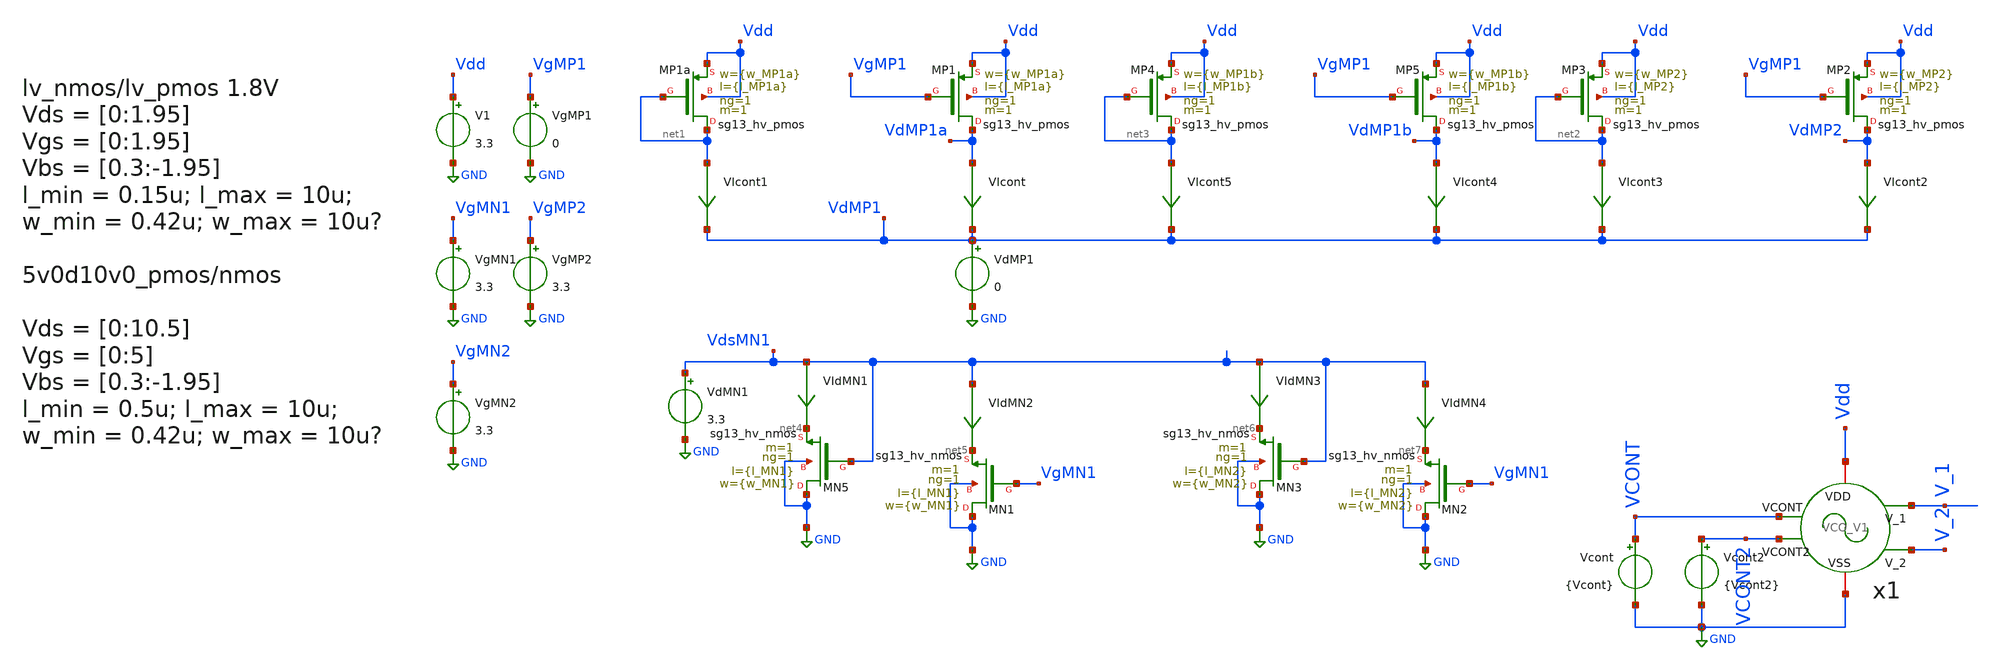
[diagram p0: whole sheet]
** sch_path: xschem/VCO/TB_VCO_Design_V1.sch
**.subckt TB_VCO_Design_V1
V1 Vdd GND 3.3
VIcont VdMP1a VdMP1 0
.save i(vicont)
VdMP1 VdMP1 GND 0
VgMP1 VgMP1 GND 0
VdMN1 VdsMN1 GND 3.3
VIdMN1 VdsMN1 net4 0
.save i(vidmn1)
VIcont1 net1 VdMP1 0
.save i(vicont1)
VIdMN2 VdsMN1 net5 0
.save i(vidmn2)
VgMN1 VgMN1 GND 3.3
VIdMN3 VdsMN1 net6 0
.save i(vidmn3)
VIdMN4 VdsMN1 net7 0
.save i(vidmn4)
VIcont2 VdMP2 VdMP1 0
.save i(vicont2)
VIcont3 net2 VdMP1 0
.save i(vicont3)
VgMP2 VgMP2 GND 3.3
VgMN2 VgMN2 GND 3.3
Vcont VCONT GND {Vcont}
XMP1a net1 net1 Vdd Vdd sg13_hv_pmos w={w_MP1a} l={l_MP1a} ng=1 m=1 mm_ok=1
XMP1 VdMP1a VgMP1 Vdd Vdd sg13_hv_pmos w={w_MP1a} l={l_MP1a} ng=1 m=1 mm_ok=1
XMP3 net2 net2 Vdd Vdd sg13_hv_pmos w={w_MP2} l={l_MP2} ng=1 m=1 mm_ok=1
XMP2 VdMP2 VgMP1 Vdd Vdd sg13_hv_pmos w={w_MP2} l={l_MP2} ng=1 m=1 mm_ok=1
XMN5 GND VdsMN1 net4 GND sg13_hv_nmos w={w_MN1} l={l_MN1} ng=1 m=1 mm_ok=1
XMN1 GND VgMN1 net5 GND sg13_hv_nmos w={w_MN1} l={l_MN1} ng=1 m=1 mm_ok=1
XMN3 GND VdsMN1 net6 GND sg13_hv_nmos w={w_MN2} l={l_MN2} ng=1 m=1 mm_ok=1
XMN2 GND VgMN1 net7 GND sg13_hv_nmos w={w_MN2} l={l_MN2} ng=1 m=1 mm_ok=1
VIcont4 VdMP1b VdMP1 0
.save i(vicont4)
VIcont5 net3 VdMP1 0
.save i(vicont5)
XMP4 net3 net3 Vdd Vdd sg13_hv_pmos w={w_MP1b} l={l_MP1b} ng=1 m=1 mm_ok=1
XMP5 VdMP1b VgMP1 Vdd Vdd sg13_hv_pmos w={w_MP1b} l={l_MP1b} ng=1 m=1 mm_ok=1
x1 VCONT GND Vdd V_1 V_2 VCONT2 VCO_V1
Vcont2 VCONT2 GND {Vcont2}
**** begin user architecture code


.save all


.csparam start = 10
.param Vcont = 1

.control

dc VdMP1 0 3.3 0.2 VgMP1 0 3.3 0.2
let IdMP1a = i(VIcont)
let IdMP1a_Diode = i(VIcont1)
let  VsdMP1 = v(Vdd) - v(VdMP1)
let VthMP1 = @n.xMP1.msky130_fd_pr__pfet_01v8[vth]
let  VovMP1a = v(Vdd) - v(VdMP1) - VthMP1
*plot IdMP1a IdMP1a_Diode vs VsdMP1
*plot IdMP1a_Diode vs VovMP1

let IdMP1b = i(VIcont4)
let IdMP1b_Diode = i(VIcont5)
let  VsdMP1 = v(Vdd) - v(VdMP1)
let VthMP1 = @n.xMP1.msky130_fd_pr__pfet_01v8[vth]
let  VovMP1b = v(Vdd) - v(VdMP1) - VthMP1
*plot IdMP1b IdMP1b_Diode vs VsdMP1
*plot IdMP1b_Diode vs VovMP1

let IdMP2 = i(VIcont2)
let IdMP2_Diode = i(VIcont3)
let  VsdMP2 = v(Vdd) - v(VdMP2)
let VthMP2 = @m.xMP4.msky130_fd_pr__pfet_01v8[vth]
let  VovMP2 = v(Vdd) - v(VdMP2) - VthMP2
*plot IdMP2 IdMP2_Diode vs VsdMP2
*plot IdMP2_Diode vs VovMP2
let KP1 = IdMP1_Diode/(VovMP1*VovMP1)
let AP1 = sqrt(KP1)
let KP2 = IdMP2_Diode/(VovMP2*VovMP2)
let AP2 = sqrt(KP2)

plot AP1 AP2

*plot IdMP1_Diode IdMP2_Diode vs VsdMP1
print VthMP1 VthMP2
*wrdata ../../sim_data/data_VCO_design.txt IdMP1_Diode VovMP1 IdMP1 vs VsdMP1
wrdata
+ /workspaces/usm-vlsi-tools/shared_xserver/simulations/SKY130/IPD500-TimebasedDCDCBuck/sim_data/data_VCO_design.txt IdMP1_Diode VovMP1 IdMP1 vs VsdMP1
wrdata
+ /workspaces/usm-vlsi-tools/shared_xserver/simulations/SKY130/IPD500-TimebasedDCDCBuck/sim_data/data_AP1_VthMP1.txt AP1 VthMP1 AP2 VthMP2

reset
*load save_data.raw
*show

dc VdMN1 0 3.3 0.2 VgMN1 0 3.3 0.2
let VdsMN1 = v(VdsMN1)
let IdMN1_Diode = i(VIdMN1)
let IdMN1 = i(VIdMN2)
let VthMN1 = @m.xMN1.msky130_fd_pr__nfet_01v8[vth]
let VovMN1 = VdsMN1 - VthMN1
*plot IdMN1 IdMN1_Diode vs VdsMN1
*plot IdMN1_Diode vs VovMN1

let VdsMN2 = v(VdsMN1)
let IdMN2_Diode = i(VIdMN3)
let IdMN2 = i(VIdMN4)
let VthMN2 = @m.xMN4.msky130_fd_pr__nfet_01v8[vth]
let VovMN2 = VdsMN2 - VthMN2
*plot IdMN2 IdMN2_Diode vs VdsMN2
*plot IdMN2_Diode vs VovMN2

let KN1 = IdMN1_Diode/(VovMN1*VovMN1)
let AN1 = sqrt(KN1)
let KN2 = IdMN2_Diode/(VovMN2*VovMN2)
let AN2 = sqrt(KN2)
*plot AN1 AN2
print VthMN1 VthMN2
wrdata
+ /workspaces/usm-vlsi-tools/shared_xserver/simulations/SKY130/IPD500-TimebasedDCDCBuck/sim_data/data_AN1_VthMN1.txt AN1 VthMN1


reset

dc Vcont 0 2 0.1
*dc Vcont 0 3 0.1
let Icont = i(v.x1.x1.VIcont)
let Icont2 = i(v.x1.x1.VIcont1)
let Icont3 = i(v.x1.x1.VIcont3)
let VCN = v(x1.x1.VCN)
let VCP = v(x1.x1.VCP)
let Vsg_MP3 = v(Vdd) - VCP
let VsdMP3 = v(VDD) - v(x1.x1.VSMP4)
let VdsMN3 = v(x1.x1.VdsMN3)


plot Icont Icont2 Icont3 vs Vcont
plot Icont3 vs Vcont
plot Icont3 vs VCP
plot VCP vs Vcont
plot VCN Vsg_MP3 vs Vcont
plot VsdMP3 VdsMN3 vs Vcont
*plot Vin vs Vcont
.endc





.lib cornerMOShv.lib mos_tt
.lib cornerMOSlv.lib mos_tt
*.lib cornerMOShv.lib mos_ff
*.lib cornerMOSlv.lib mos_ff
*.lib cornerMOShv.lib mos_ss
*.lib cornerMOSlv.lib mos_ss
*.lib cornerMOShv.lib mos_sf
*.lib cornerMOSlv.lib mos_sf
*.lib cornerMOShv.lib mos_fs
*.lib cornerMOSlv.lib mos_fs

*.include /opt/pdks/ihp-sg13g2/libs.ref/sg13g2_stdcell/spice/sg13g2_stdcell.spice
*.lib $::SG13G2_MODELS/cornerRES.lib res_typ
*.lib $::SG13G2_MODELS/cornerCAP.lib cap_typ
*.lib $::SG13G2_MODELS/diodes.lib


.param Vcont2 = 3.3

.param w_MP1a = 4u
.param l_MP1a = 7u
.param w_MP1b = 4u
.param l_MP1b = 7u
.param w_MP2 = 8u
.param l_MP2 = 4u
.param w_MP3 = 5u
.param l_MP3 = 4u
.param w_MP4 = 5u
.param l_MP4 = 5u

.param w_MN1 = 5u
.param l_MN1 = 0.5u
.param w_MN2 = 5u
.param l_MN2 = 0.5u
.param w_MN3 = 3u
.param l_MN3 = 0.5u
.param w_MN4 = 2u
.param l_MN4 = 5u





.save all
.param Vcont = 1

.control
reset
unset filetype
op
alter Vcont 1
let VCN = v(x1.x1.VCN)
let VCP = v(x1.x1.VCP)

let Vsd_MP4 = v(x1.x1.VSMP4) - v(x1.x1.VOUT)
let Vsd_MP3 = v(VDD) - v(x1.x1.VSMP4)
let Vsd_MP2 = v(VDD) - v(x1.x1.VCP)
let Vsd_MP1 = v(VDD) - VCN
let Vds_MN4 = v(x1.x1.VOUT) - v(x1.x1.VdsMN3)

let Vth_MP1a = @n.x1.x1.xmp1a.nsg13_hv_pmos[vth]
let Vth_MP1b = @n.x1.x1.xmp1b.nsg13_hv_pmos[vth]
let Vth_MP2 = @n.x1.x1.xmp2.nsg13_hv_pmos[vth]
let Vth_MP3 = @n.x1.x1.xmp3.nsg13_hv_pmos[vth]
let Vth_MP4 = @n.x1.x1.xmp3.nsg13_hv_pmos[vth]
let Vth_MN1 = @n.x1.x1.xmn1.nsg13_hv_nmos[vth]
let Vth_MN2 = @n.x1.x1.xmn2.nsg13_hv_nmos[vth]
let Vth_MN3 = @n.x1.x1.xmn3.nsg13_hv_nmos[vth]
let Vth_MN4 = @n.x1.x1.xmn4.nsg13_hv_nmos[vth]

let Vsg_MP4 = v(x1.x1.VSMP4) - v(x1.x1.VIN)
let Vsg_MP3 = v(VDD) - VCP
let Vsg_MP1a = v(VDD) - v(VCONT)
let Vsg_MP1b = v(VDD) - v(VCONT2)
let Vgs_MN4 = v(x1.x1.VIN) - v(x1.x1.VdsMN3)

let Vov_MP1a = Vsg_MP1a - Vth_MP1a
let Vov_MP1b = Vsg_MP1b - Vth_MP1b
let Vov_MP3 = Vsg_MP3 - Vth_MP3
let Vov_MP4 = Vsg_MP4 - Vth_MP4
let Vov_MN2 =  VCN - Vth_MN2
let Vov_MN3 =  VCN - Vth_MN3
let Vov_MN4 =  VCN - Vth_MN4

let gds_MN3 = @n.x1.x1.xmn3.nsg13_hv_nmos[gds]
let Ron_MN3 = 1/gds_MN3
let gds_MP3 = @n.x1.x1.xmp3.nsg13_hv_pmos[gds]
let Ron_MP3 = 1/gds_MP3


write TB_VCO_Design_V1.raw
.endc



**** end user architecture code
**.ends

* expanding   symbol:
*+  /workspaces/usm-vlsi-tools/shared_xserver/simulations/Projects/IHP/IPD500_TD_Buck/xschem/VCO/VCO_V1.sym # of pins=6
** sym_path: xschem/VCO/VCO_V1.sym
** sch_path: xschem/VCO/VCO_V1.sch
.subckt VCO_V1 VCONT VSS VDD V_1 V_2 VCONT2
*.ipin VCONT
*.iopin VDD
*.iopin VSS
*.opin V_1
*.opin V_2
*.ipin VCONT2
x1 VDD VCONT V_1 V_5 VSS VCONT2 stage_V1
x2 VDD VCONT V_2 V_1 VSS VCONT2 stage_V1
x3 VDD VCONT V_3 V_2 VSS VCONT2 stage_V1
x4 VDD VCONT V_4 V_3 VSS VCONT2 stage_V1
x5 VDD VCONT V_5 V_4 VSS VCONT2 stage_V1
.ends


* expanding   symbol:  ../VCO/stage_V1.sym # of pins=6
** sym_path: xschem/VCO/stage_V1.sym
** sch_path: xschem/VCO/stage_V1.sch
.subckt stage_V1 VDD VCONT VOUT VIN VSS VCONT2
*.ipin VCONT2
*.ipin VIN
*.opin VOUT
*.iopin VDD
*.iopin VSS
*.ipin VCONT
XMN1 VSS net2 net2 VSS sg13_hv_nmos w={w_MN1} l={l_MN1} ng=1 m={m_MN1} mm_ok=1
XMN2 VSS net2 net3 VSS sg13_hv_nmos w={w_MN2} l={l_MN2} ng=1 m={m_MN2} mm_ok=1
XMN3 VSS net2 VdsMN3 VSS sg13_hv_nmos w={w_MN3} l={l_MN3} ng=1 m={m_MN3} mm_ok=1
XMP1a VCN VCONT VDD VDD sg13_hv_pmos w={w_MP1a} l={l_MP1a} ng=1 m={m_MP1a} mm_ok=1
XMP2 VCP VCP VDD VDD sg13_hv_pmos w={w_MP2} l={l_MP2} ng=1 m={m_MP2} mm_ok=1
XMP3 net4 VCP VDD VDD sg13_hv_pmos w={w_MP3} l={l_MP3} ng=1 m={m_MP3} mm_ok=1
XMP7 net1 VIN VSMP4 VDD sg13_hv_pmos w={w_MP4} l={l_MP4} ng=1 m={m_MP4} mm_ok=1
XMN4 VdsMN3 VIN net1 VSS sg13_hv_nmos w={w_MN4} l={l_MN4} ng=1 m={m_MN4} mm_ok=1
XMP1b VCN VCONT2 VDD VDD sg13_hv_pmos w={w_MP1b} l={l_MP1b} ng=1 m={m_MP1b} mm_ok=1
VIcont1 VCN net2 0
.save i(vicont1)
VIcont2 VCP net3 0
.save i(vicont2)
VIcont3 net4 VSMP4 0
.save i(vicont3)
VIcont4 net1 VOUT 0
.save i(vicont4)
.ends

.GLOBAL GND
.end
